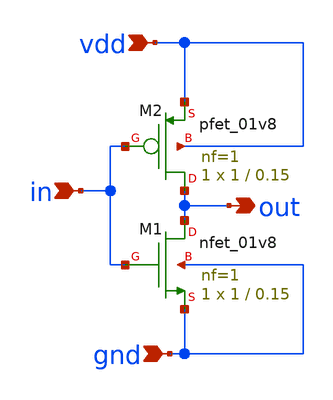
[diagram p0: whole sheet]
** sch_path: inverter/modul_inv.sch
**.subckt modul_inv vdd gnd in out
*.ipin vdd
*.ipin gnd
*.ipin in
*.opin out
XM1 out in gnd gnd sky130_fd_pr__nfet_01v8 L=0.15 W=1 nf=1 ad='int((nf+1)/2) * W/nf * 0.29' as='int((nf+2)/2) * W/nf * 0.29'
+ pd='2*int((nf+1)/2) * (W/nf + 0.29)' ps='2*int((nf+2)/2) * (W/nf + 0.29)' nrd='0.29 / W' nrs='0.29 / W'
+ sa=0 sb=0 sd=0 mult=1 m=1
XM2 out in vdd vdd sky130_fd_pr__pfet_01v8 L=0.15 W=1 nf=1 ad='int((nf+1)/2) * W/nf * 0.29' as='int((nf+2)/2) * W/nf * 0.29'
+ pd='2*int((nf+1)/2) * (W/nf + 0.29)' ps='2*int((nf+2)/2) * (W/nf + 0.29)' nrd='0.29 / W' nrs='0.29 / W'
+ sa=0 sb=0 sd=0 mult=1 m=1
**.ends
.end
